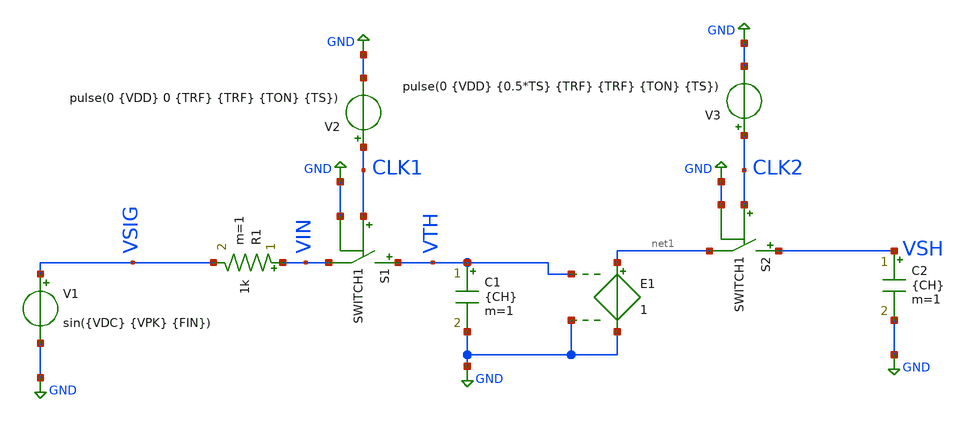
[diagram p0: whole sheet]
** sch_path: Designs/lab_02_tah_sah_tb.sch
**.subckt lab_02_tah_sah_tb
V1 VSIG GND sin({VDC} {VPK} {FIN})
R1 VIN VSIG 1k m=1
V2 CLK1 GND pulse(0 {VDD} 0 {TRF} {TRF} {TON} {TS})
C1 VTH GND {CH} m=1
S1 VTH VIN CLK1 GND SWITCH1
S2 VSH net1 CLK2 GND SWITCH1
V3 CLK2 GND pulse(0 {VDD} {0.5*TS} {TRF} {TRF} {TON} {TS})
C2 VSH GND {CH} m=1
E1 net1 GND VTH GND 1
**** begin user architecture code


*Required model for the switch
.model SWITCH1 sw vt={VDD/2}
*These are the values of the parameters to be used
.param TS=1u
.param CH=1p CP={0.1*CH} RSIG=1k TON={0.4*TS} TRF=1n NCYC=5.5 NFFT=256 FIN={(NCYC/NFFT)/TS}
.param VDD=2 VDC={VDD/2} VCM={VDD/2} VPK={VDD/4} TDROP={0.5/FIN} TSTOP={(NCYC/FIN)+TDROP}
*Analysis setup and control statements

.tran 25n {TSTOP} {TDROP}
*save all voltages and currents
.save all
*options for an accurate precision output and to allow raw files to be ascii
.options filetype=ascii
.options reltol=1u vntol=1u abstol=1p


**** end user architecture code
**.ends
.GLOBAL GND
.end
